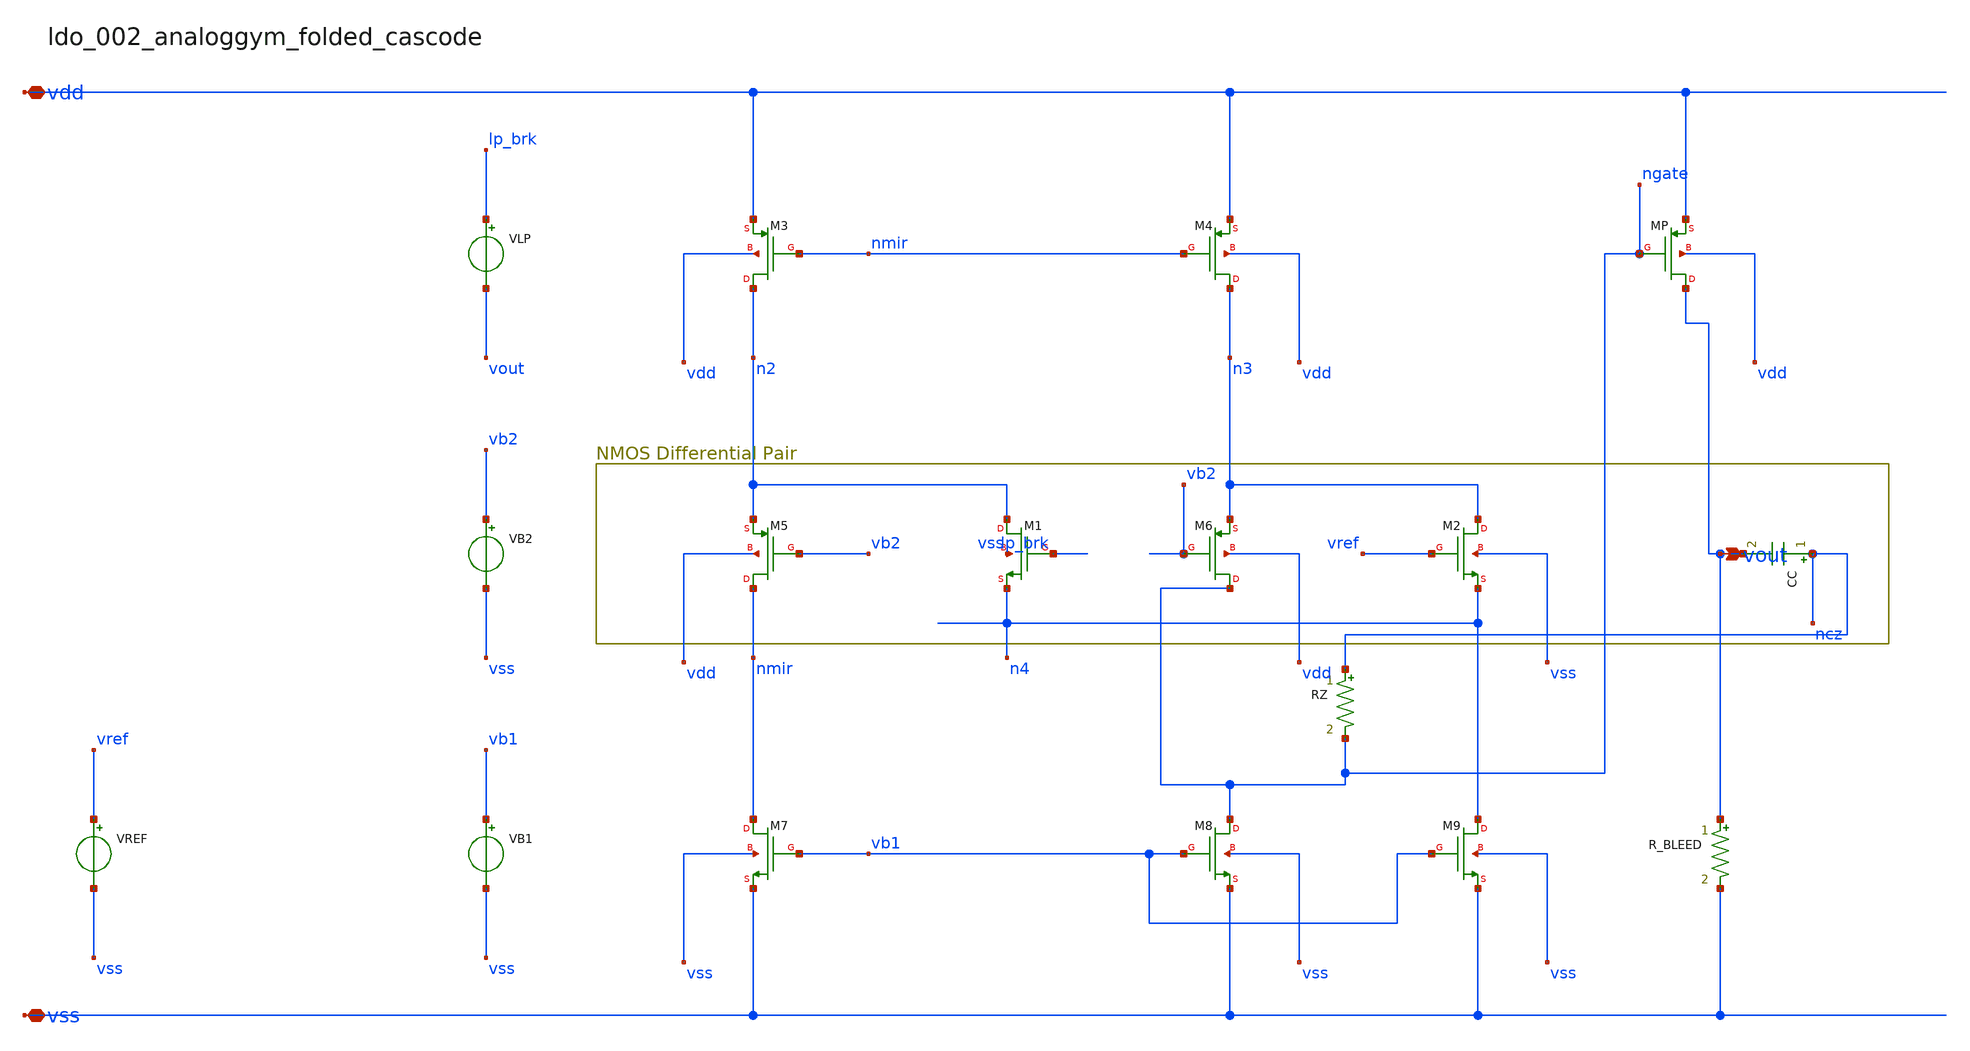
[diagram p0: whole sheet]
** sch_path: analog-db/raw/ldo_002_analoggym_folded_cascode/ldo_002_analoggym_folded_cascode_annotated.sch
**.subckt ldo_002_analoggym_folded_cascode_annotated vdd vss vout
*.iopin vdd
*.iopin vss
*.opin vout
CC ncz vout 'c_comp' m=1
RZ ncz ngate 'r_z' m=1
R_BLEED vout vss 'r_bleed' m=1
VB1 vb1 vss dc {vb1_val}
VB2 vb2 vss dc {vb2_val}
VLP lp_brk vout dc 0
VREF vref vss dc {vref_val}
XM1 n2 lp_brk n4 vss sg13_hv_nmos w=x_dut_xm1_w l=x_dut_xm1_l ng=1 m=1
XM2 n3 vref n4 vss sg13_hv_nmos w=x_dut_xm2_w l=x_dut_xm2_l ng=1 m=1
XM3 n2 nmir vdd vdd sg13_hv_pmos w=x_dut_xm3_w l=x_dut_xm3_l ng=1 m=1
XM4 n3 nmir vdd vdd sg13_hv_pmos w=x_dut_xm4_w l=x_dut_xm4_l ng=1 m=1
XM5 nmir vb2 n2 vdd sg13_hv_pmos w=x_dut_xm5_w l=x_dut_xm5_l ng=1 m=1
XM6 ngate vb2 n3 vdd sg13_hv_pmos w=x_dut_xm6_w l=x_dut_xm6_l ng=1 m=1
XM7 nmir vb1 vss vss sg13_hv_nmos w=x_dut_xm7_w l=x_dut_xm7_l ng=1 m=1
XM8 ngate vb1 vss vss sg13_hv_nmos w=x_dut_xm8_w l=x_dut_xm8_l ng=1 m=1
XM9 n4 vb1 vss vss sg13_hv_nmos w=x_dut_xm9_w l=x_dut_xm9_l ng=1 m=1
XMP vout ngate vdd vdd sg13_hv_pmos w=x_dut_xmp_w l=x_dut_xmp_l ng=1 m=x_dut_xmp_m
**.ends
.end
